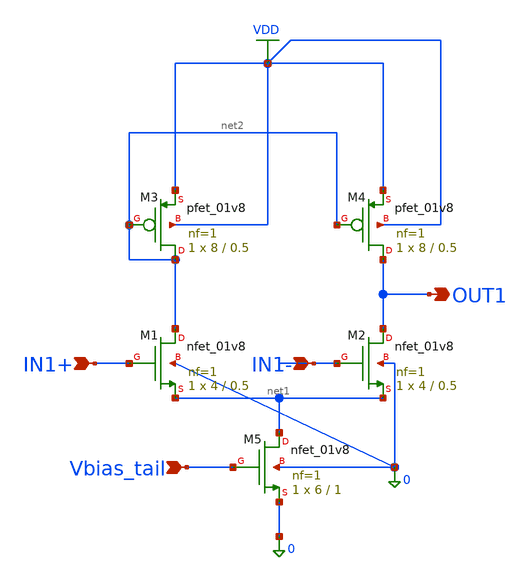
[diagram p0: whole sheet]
** sch_path: ota_core.sch
**.subckt ota_core IN1+ IN1- OUT1 Vbias_tail
*.ipin IN1+
*.ipin IN1-
*.opin OUT1
*.ipin Vbias_tail
XM1 net2 IN1+ net1 0 sky130_fd_pr__nfet_01v8 L=0.5 W=4 nf=1 ad='int((1 + 1)/2) * 4 / 1 * 0.29' as='int((1 + 2)/2) * 4 / 1 * 0.29'
+ pd='2*int((1 + 1)/2) * (4 / 1 + 0.29)' ps='2*int((1 + 2)/2) * (4 / 1 + 0.29)' nrd='0.29 / 4 ' nrs='0.29 / 4 '
+ sa=0 sb=0 sd=0 mult=1 m=1
XM2 OUT1 IN1- net1 0 sky130_fd_pr__nfet_01v8 L=0.5 W=4 nf=1 ad='int((1 + 1)/2) * 4 / 1 * 0.29' as='int((1 + 2)/2) * 4 / 1 * 0.29'
+ pd='2*int((1 + 1)/2) * (4 / 1 + 0.29)' ps='2*int((1 + 2)/2) * (4 / 1 + 0.29)' nrd='0.29 / 4 ' nrs='0.29 / 4 '
+ sa=0 sb=0 sd=0 mult=1 m=1
XM3 net2 net2 VDD VDD sky130_fd_pr__pfet_01v8 L=0.5 W=8 nf=1 ad='int((1 + 1)/2) * 8 / 1 * 0.29' as='int((1 + 2)/2) * 8 / 1 * 0.29'
+ pd='2*int((1 + 1)/2) * (8 / 1 + 0.29)' ps='2*int((1 + 2)/2) * (8 / 1 + 0.29)' nrd='0.29 / 8 ' nrs='0.29 / 8 '
+ sa=0 sb=0 sd=0 mult=1 m=1
XM4 OUT1 net2 VDD VDD sky130_fd_pr__pfet_01v8 L=0.5 W=8 nf=1 ad='int((1 + 1)/2) * 8 / 1 * 0.29' as='int((1 + 2)/2) * 8 / 1 * 0.29'
+ pd='2*int((1 + 1)/2) * (8 / 1 + 0.29)' ps='2*int((1 + 2)/2) * (8 / 1 + 0.29)' nrd='0.29 / 8 ' nrs='0.29 / 8 '
+ sa=0 sb=0 sd=0 mult=1 m=1
XM5 net1 Vbias_tail 0 0 sky130_fd_pr__nfet_01v8 L=1 W=6 nf=1 ad='int((1 + 1)/2) * 6 / 1 * 0.29' as='int((1 + 2)/2) * 6 / 1 * 0.29'
+ pd='2*int((1 + 1)/2) * (6 / 1 + 0.29)' ps='2*int((1 + 2)/2) * (6 / 1 + 0.29)' nrd='0.29 / 6 ' nrs='0.29 / 6 '
+ sa=0 sb=0 sd=0 mult=1 m=1
**.ends
.GLOBAL VDD
.end
